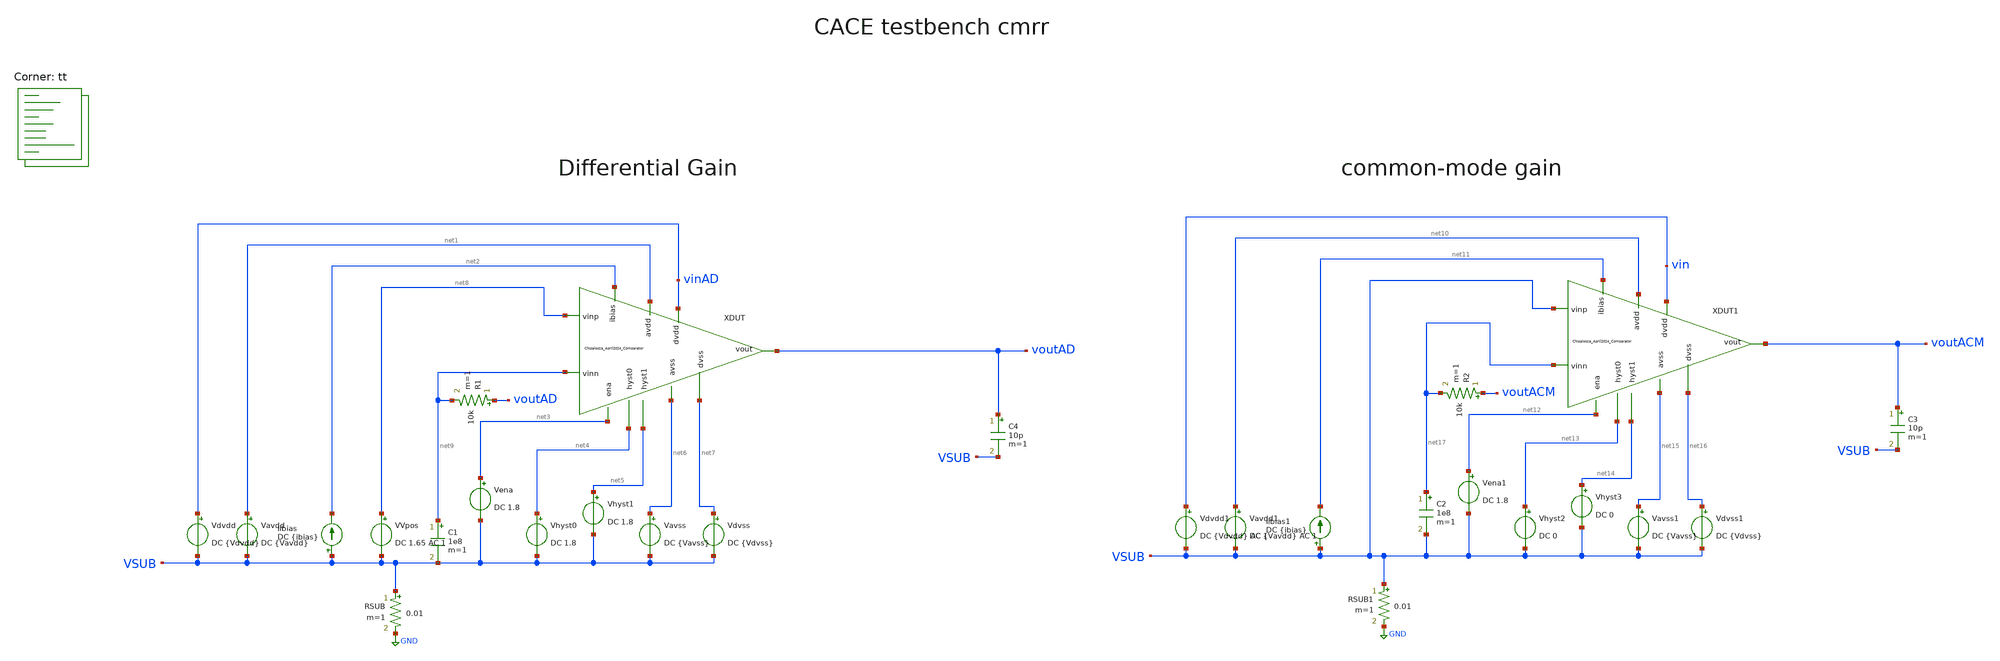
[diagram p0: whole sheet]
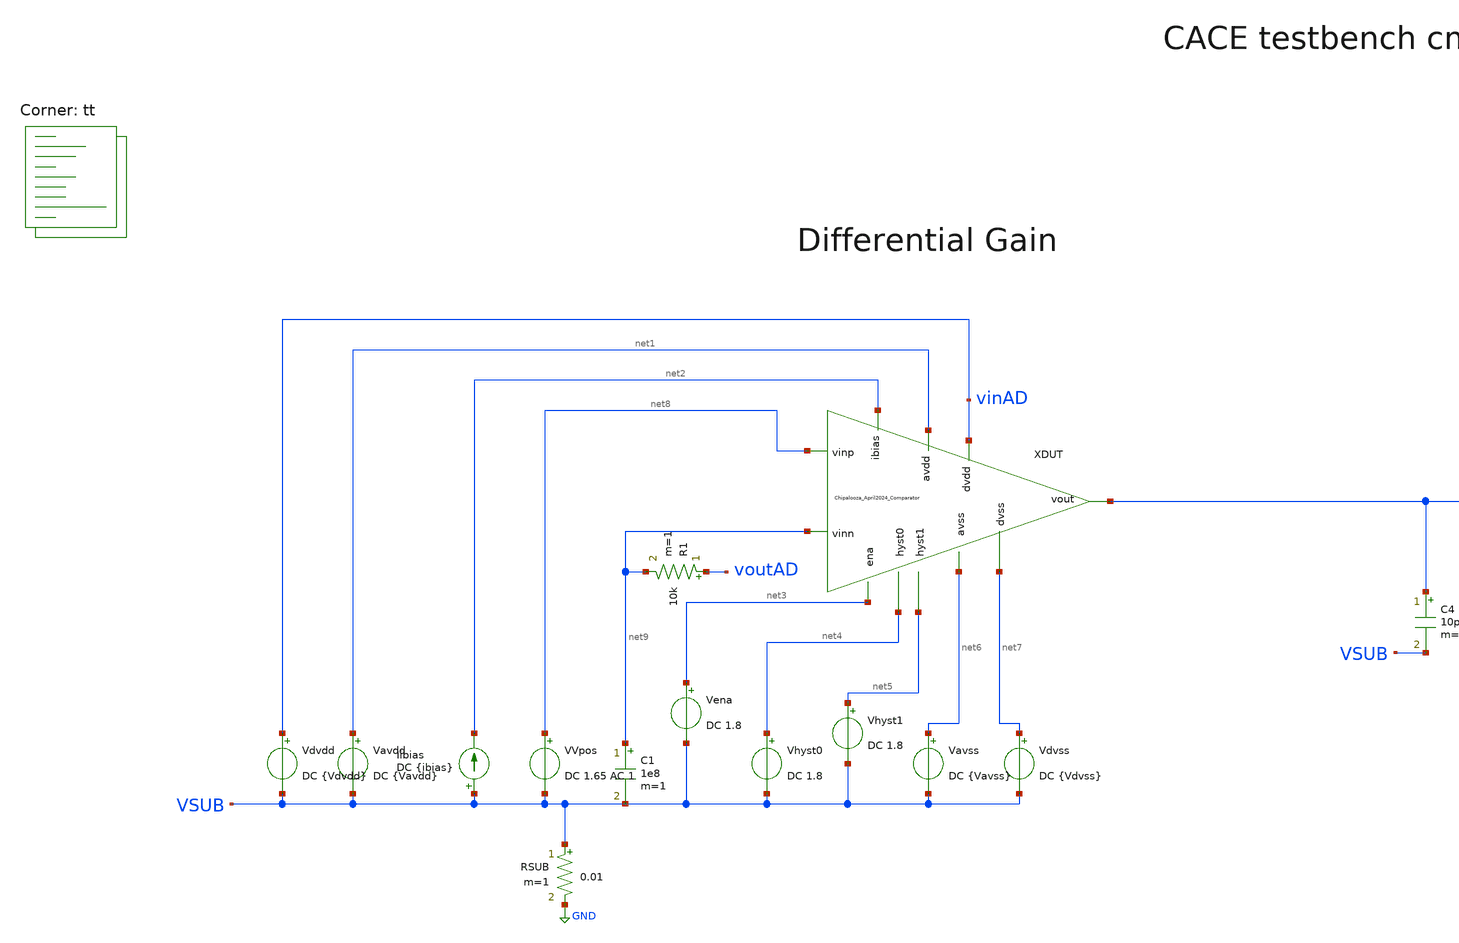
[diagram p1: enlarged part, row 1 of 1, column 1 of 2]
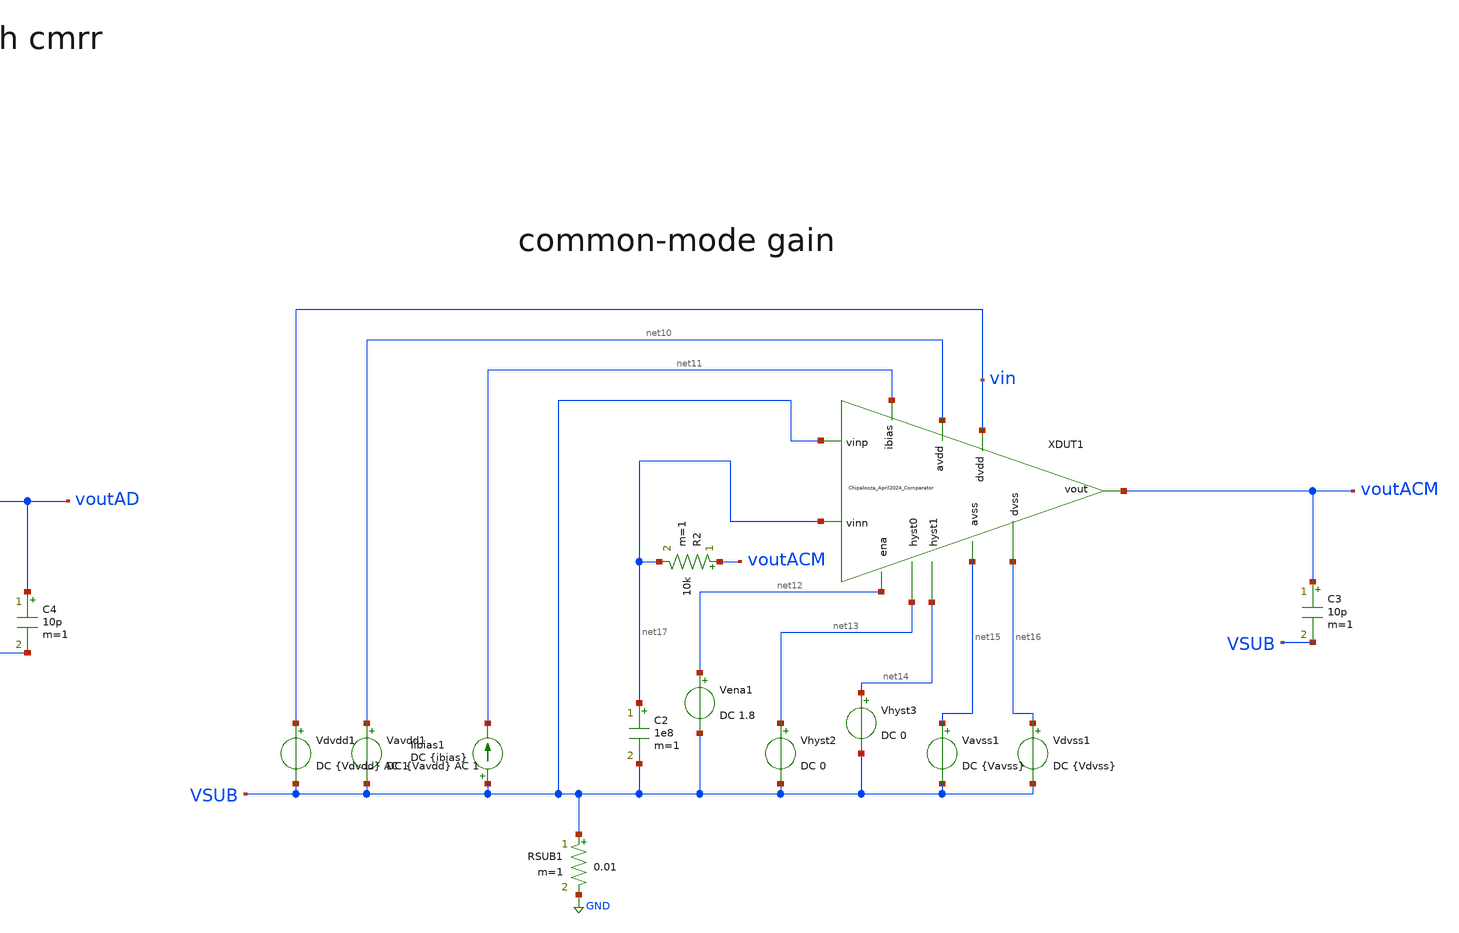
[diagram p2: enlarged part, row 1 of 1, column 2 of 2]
** sch_path: Chipalooza_April2024_Comparator/xschem/TB_psrr.sch
**.subckt TB_psrr
Vavdd net1 VSUB DC {Vavdd}
Vdvdd vinAD VSUB DC {Vdvdd}
Vena net3 VSUB DC 1.8
Vhyst0 net4 VSUB DC 1.8
Vhyst1 net5 VSUB DC 1.8
Vavss net6 VSUB DC {Vavss}
Vdvss net7 VSUB DC {Vdvss}
RSUB VSUB GND 0.01 m=1
Iibias VSUB net2 DC {ibias}
XDUT net4 net5 net1 net8 net6 net9 vinAD net7 voutAD net2 net3 Chipalooza_April2024_Comparator
VVpos net8 VSUB DC 1.65 AC 1
C1 net9 VSUB 1e8 m=1
R1 voutAD net9 10k m=1
C4 voutAD VSUB 10p m=1
Vavdd1 net10 VSUB DC {Vavdd} AC 1
Vdvdd1 vin VSUB DC {Vdvdd} AC 1
Vena1 net12 VSUB DC 1.8
Vhyst2 net13 VSUB DC 0
Vhyst3 net14 VSUB DC 0
Vavss1 net15 VSUB DC {Vavss}
Vdvss1 net16 VSUB DC {Vdvss}
RSUB1 VSUB GND 0.01 m=1
Iibias1 VSUB net11 DC {ibias}
XDUT1 net13 net14 net10 VSUB net15 net17 vin net16 voutACM net11 net12
+ Chipalooza_April2024_Comparator
C3 voutACM VSUB 10p m=1
R2 voutACM net17 10k m=1
C2 net17 VSUB 1e8 m=1
**** begin user architecture code
.lib $::SKYWATER_MODELS/sky130.lib.spice tt

* this option enables mos model bin
* selection based on W/NF instead of W
*.option wnflag=1
.option savecurrents
.option save all
.option temp=25

.control

.param vdvdd=1.8 vavdd=3.3 rout=0 cout=1f
.param ibias=1u ena=1 Vhyst_0=1 Vhyst_1=1
.param vavss=0 vdvss=0


ac dec 20 1 1e12
plot V(voutACM)
plot db(V(voutACM))
plot db((V(voutACM)-V(voutAD))/(V(vin)-V(vinAD)))

write TB_cmrr.raw


*quit 0

.endc


**** end user architecture code
**.ends

* expanding   symbol:  Chipalooza_April2024_Comparator.sym # of pins=11
** sym_path: Chipalooza_April2024_Comparator/xschem/Chipalooza_April2024_Comparator.sym
** sch_path: Chipalooza_April2024_Comparator/xschem/Chipalooza_April2024_Comparator.sch
.subckt Chipalooza_April2024_Comparator hyst0 hyst1 avdd vinp avss vinn dvdd dvss vout ibias ena
*.ipin vinp
*.ipin vinn
*.ipin hyst0
*.ipin hyst1
*.ipin avdd
*.ipin avss
*.ipin dvdd
*.ipin dvss
*.opin vout
*.ipin ena
*.ipin ibias
XM29 SumOutBar SumOut dvdd dvdd sky130_fd_pr__pfet_01v8 L=1 W=4 nf=1 ad='int((nf+1)/2) * W/nf * 0.29'
+ as='int((nf+2)/2) * W/nf * 0.29' pd='2*int((nf+1)/2) * (W/nf + 0.29)' ps='2*int((nf+2)/2) * (W/nf + 0.29)'
+ nrd='0.29 / W' nrs='0.29 / W' sa=0 sb=0 sd=0 mult=2 m=2
XM30 SumOutBar SumOut avssi dvss sky130_fd_pr__nfet_01v8 L=1 W=2 nf=1 ad='int((nf+1)/2) * W/nf * 0.29'
+ as='int((nf+2)/2) * W/nf * 0.29' pd='2*int((nf+1)/2) * (W/nf + 0.29)' ps='2*int((nf+2)/2) * (W/nf + 0.29)'
+ nrd='0.29 / W' nrs='0.29 / W' sa=0 sb=0 sd=0 mult=2 m=2
XM25 net3 ibias avssi avss sky130_fd_pr__nfet_g5v0d10v5 L=4 W=1 nf=1 ad='int((nf+1)/2) * W/nf * 0.29'
+ as='int((nf+2)/2) * W/nf * 0.29' pd='2*int((nf+1)/2) * (W/nf + 0.29)' ps='2*int((nf+2)/2) * (W/nf + 0.29)'
+ nrd='0.29 / W' nrs='0.29 / W' sa=0 sb=0 sd=0 mult=2 m=2
C1 avss 0 2p m=1
XM39 net4 ibias avssi avss sky130_fd_pr__nfet_g5v0d10v5 L=1 W=1 nf=1 ad='int((nf+1)/2) * W/nf * 0.29'
+ as='int((nf+2)/2) * W/nf * 0.29' pd='2*int((nf+1)/2) * (W/nf + 0.29)' ps='2*int((nf+2)/2) * (W/nf + 0.29)'
+ nrd='0.29 / W' nrs='0.29 / W' sa=0 sb=0 sd=0 mult=2 m=2
XM16 vout SumOutBar dvdd dvdd sky130_fd_pr__pfet_01v8 L=1 W=4 nf=1 ad='int((nf+1)/2) * W/nf * 0.29' as='int((nf+2)/2) * W/nf * 0.29'
+ pd='2*int((nf+1)/2) * (W/nf + 0.29)' ps='2*int((nf+2)/2) * (W/nf + 0.29)' nrd='0.29 / W' nrs='0.29 / W'
+ sa=0 sb=0 sd=0 mult=2 m=2
XM18 vout SumOutBar avssi dvss sky130_fd_pr__nfet_01v8 L=1 W=2 nf=1 ad='int((nf+1)/2) * W/nf * 0.29'
+ as='int((nf+2)/2) * W/nf * 0.29' pd='2*int((nf+1)/2) * (W/nf + 0.29)' ps='2*int((nf+2)/2) * (W/nf + 0.29)'
+ nrd='0.29 / W' nrs='0.29 / W' sa=0 sb=0 sd=0 mult=2 m=2
XM4 SourceBias2 SourceBias2 avdd avdd sky130_fd_pr__pfet_g5v0d10v5 L=1 W=48 nf=1 ad='int((nf+1)/2) * W/nf * 0.29'
+ as='int((nf+2)/2) * W/nf * 0.29' pd='2*int((nf+1)/2) * (W/nf + 0.29)' ps='2*int((nf+2)/2) * (W/nf + 0.29)'
+ nrd='0.29 / W' nrs='0.29 / W' sa=0 sb=0 sd=0 mult=2 m=2
XM5 N1 SourceBias2 avdd avdd sky130_fd_pr__pfet_g5v0d10v5 L=1 W=48 nf=1 ad='int((nf+1)/2) * W/nf * 0.29'
+ as='int((nf+2)/2) * W/nf * 0.29' pd='2*int((nf+1)/2) * (W/nf + 0.29)' ps='2*int((nf+2)/2) * (W/nf + 0.29)'
+ nrd='0.29 / W' nrs='0.29 / W' sa=0 sb=0 sd=0 mult=2 m=2
XM6 N2 SourceBias2 avdd avdd sky130_fd_pr__pfet_g5v0d10v5 L=1 W=48 nf=1 ad='int((nf+1)/2) * W/nf * 0.29'
+ as='int((nf+2)/2) * W/nf * 0.29' pd='2*int((nf+1)/2) * (W/nf + 0.29)' ps='2*int((nf+2)/2) * (W/nf + 0.29)'
+ nrd='0.29 / W' nrs='0.29 / W' sa=0 sb=0 sd=0 mult=2 m=2
XM7 SumOut net5 N2 avdd sky130_fd_pr__pfet_g5v0d10v5 L=1 W=48 nf=1 ad='int((nf+1)/2) * W/nf * 0.29' as='int((nf+2)/2) * W/nf * 0.29'
+ pd='2*int((nf+1)/2) * (W/nf + 0.29)' ps='2*int((nf+2)/2) * (W/nf + 0.29)' nrd='0.29 / W' nrs='0.29 / W'
+ sa=0 sb=0 sd=0 mult=2 m=2
XM8 Sum net5 N1 avdd sky130_fd_pr__pfet_g5v0d10v5 L=1 W=48 nf=1 ad='int((nf+1)/2) * W/nf * 0.29' as='int((nf+2)/2) * W/nf * 0.29'
+ pd='2*int((nf+1)/2) * (W/nf + 0.29)' ps='2*int((nf+2)/2) * (W/nf + 0.29)' nrd='0.29 / W' nrs='0.29 / W'
+ sa=0 sb=0 sd=0 mult=2 m=2
XM9 SumOut net6 P2 avss sky130_fd_pr__nfet_g5v0d10v5 L=3 W=12 nf=1 ad='int((nf+1)/2) * W/nf * 0.29' as='int((nf+2)/2) * W/nf * 0.29'
+ pd='2*int((nf+1)/2) * (W/nf + 0.29)' ps='2*int((nf+2)/2) * (W/nf + 0.29)' nrd='0.29 / W' nrs='0.29 / W'
+ sa=0 sb=0 sd=0 mult=2 m=2
XM10 Sum net6 P1 avss sky130_fd_pr__nfet_g5v0d10v5 L=3 W=12 nf=1 ad='int((nf+1)/2) * W/nf * 0.29' as='int((nf+2)/2) * W/nf * 0.29'
+ pd='2*int((nf+1)/2) * (W/nf + 0.29)' ps='2*int((nf+2)/2) * (W/nf + 0.29)' nrd='0.29 / W' nrs='0.29 / W'
+ sa=0 sb=0 sd=0 mult=2 m=2
XM11 P2 Sum avssi avss sky130_fd_pr__nfet_g5v0d10v5 L=3 W=12 nf=1 ad='int((nf+1)/2) * W/nf * 0.29' as='int((nf+2)/2) * W/nf * 0.29'
+ pd='2*int((nf+1)/2) * (W/nf + 0.29)' ps='2*int((nf+2)/2) * (W/nf + 0.29)' nrd='0.29 / W' nrs='0.29 / W'
+ sa=0 sb=0 sd=0 mult=2 m=2
XM12 P1 Sum avssi avss sky130_fd_pr__nfet_g5v0d10v5 L=3 W=12 nf=1 ad='int((nf+1)/2) * W/nf * 0.29' as='int((nf+2)/2) * W/nf * 0.29'
+ pd='2*int((nf+1)/2) * (W/nf + 0.29)' ps='2*int((nf+2)/2) * (W/nf + 0.29)' nrd='0.29 / W' nrs='0.29 / W'
+ sa=0 sb=0 sd=0 mult=2 m=2
XM2 P2 vinn psource_input avdd sky130_fd_pr__pfet_g5v0d10v5 L=1 W=16 nf=1 ad='int((nf+1)/2) * W/nf * 0.29'
+ as='int((nf+2)/2) * W/nf * 0.29' pd='2*int((nf+1)/2) * (W/nf + 0.29)' ps='2*int((nf+2)/2) * (W/nf + 0.29)'
+ nrd='0.29 / W' nrs='0.29 / W' sa=0 sb=0 sd=0 mult=2 m=2
XM3 P1 vinp psource_input avdd sky130_fd_pr__pfet_g5v0d10v5 L=1 W=16 nf=1 ad='int((nf+1)/2) * W/nf * 0.29'
+ as='int((nf+2)/2) * W/nf * 0.29' pd='2*int((nf+1)/2) * (W/nf + 0.29)' ps='2*int((nf+2)/2) * (W/nf + 0.29)'
+ nrd='0.29 / W' nrs='0.29 / W' sa=0 sb=0 sd=0 mult=2 m=2
XM14 psource_input pbias_tail avdd avdd sky130_fd_pr__pfet_g5v0d10v5 L=1 W=12 nf=1 ad='int((nf+1)/2) * W/nf * 0.29'
+ as='int((nf+2)/2) * W/nf * 0.29' pd='2*int((nf+1)/2) * (W/nf + 0.29)' ps='2*int((nf+2)/2) * (W/nf + 0.29)'
+ nrd='0.29 / W' nrs='0.29 / W' sa=0 sb=0 sd=0 mult=2 m=2
XM15 pbias_tail pbias_tail avdd avdd sky130_fd_pr__pfet_g5v0d10v5 L=1 W=6 nf=1 ad='int((nf+1)/2) * W/nf * 0.29'
+ as='int((nf+2)/2) * W/nf * 0.29' pd='2*int((nf+1)/2) * (W/nf + 0.29)' ps='2*int((nf+2)/2) * (W/nf + 0.29)'
+ nrd='0.29 / W' nrs='0.29 / W' sa=0 sb=0 sd=0 mult=2 m=2
XM17 nbias_tail net14 psource_input avdd sky130_fd_pr__pfet_g5v0d10v5 L=1 W=6 nf=1 ad='int((nf+1)/2) * W/nf * 0.29'
+ as='int((nf+2)/2) * W/nf * 0.29' pd='2*int((nf+1)/2) * (W/nf + 0.29)' ps='2*int((nf+2)/2) * (W/nf + 0.29)'
+ nrd='0.29 / W' nrs='0.29 / W' sa=0 sb=0 sd=0 mult=2 m=2
XM20 N1 vinp SourceBias0 avss sky130_fd_pr__nfet_g5v0d10v5 L=1 W=8 nf=1 ad='int((nf+1)/2) * W/nf * 0.29'
+ as='int((nf+2)/2) * W/nf * 0.29' pd='2*int((nf+1)/2) * (W/nf + 0.29)' ps='2*int((nf+2)/2) * (W/nf + 0.29)'
+ nrd='0.29 / W' nrs='0.29 / W' sa=0 sb=0 sd=0 mult=2 m=2
XM21 N2 vinn SourceBias0 avss sky130_fd_pr__nfet_g5v0d10v5 L=1 W=8 nf=1 ad='int((nf+1)/2) * W/nf * 0.29'
+ as='int((nf+2)/2) * W/nf * 0.29' pd='2*int((nf+1)/2) * (W/nf + 0.29)' ps='2*int((nf+2)/2) * (W/nf + 0.29)'
+ nrd='0.29 / W' nrs='0.29 / W' sa=0 sb=0 sd=0 mult=2 m=2
XM22 SourceBias0 nbias_tail avssi avss sky130_fd_pr__nfet_g5v0d10v5 L=1 W=9 nf=1 ad='int((nf+1)/2) * W/nf * 0.29'
+ as='int((nf+2)/2) * W/nf * 0.29' pd='2*int((nf+1)/2) * (W/nf + 0.29)' ps='2*int((nf+2)/2) * (W/nf + 0.29)'
+ nrd='0.29 / W' nrs='0.29 / W' sa=0 sb=0 sd=0 mult=2 m=2
XM23 nbias_tail nbias_tail avssi avss sky130_fd_pr__nfet_g5v0d10v5 L=1 W=3 nf=1 ad='int((nf+1)/2) * W/nf * 0.29'
+ as='int((nf+2)/2) * W/nf * 0.29' pd='2*int((nf+1)/2) * (W/nf + 0.29)' ps='2*int((nf+2)/2) * (W/nf + 0.29)'
+ nrd='0.29 / W' nrs='0.29 / W' sa=0 sb=0 sd=0 mult=2 m=2
XM28 pbias_tail net7 SourceBias0 avss sky130_fd_pr__nfet_g5v0d10v5 L=1 W=3 nf=1 ad='int((nf+1)/2) * W/nf * 0.29'
+ as='int((nf+2)/2) * W/nf * 0.29' pd='2*int((nf+1)/2) * (W/nf + 0.29)' ps='2*int((nf+2)/2) * (W/nf + 0.29)'
+ nrd='0.29 / W' nrs='0.29 / W' sa=0 sb=0 sd=0 mult=2 m=2
XM45 SourceBias1 ibias avssi avss sky130_fd_pr__nfet_g5v0d10v5 L=1 W=3 nf=1 ad='int((nf+1)/2) * W/nf * 0.29'
+ as='int((nf+2)/2) * W/nf * 0.29' pd='2*int((nf+1)/2) * (W/nf + 0.29)' ps='2*int((nf+2)/2) * (W/nf + 0.29)'
+ nrd='0.29 / W' nrs='0.29 / W' sa=0 sb=0 sd=0 mult=2 m=2
XM46 SourceBias1 SourceBias1 avdd avdd sky130_fd_pr__pfet_g5v0d10v5 L=1 W=6 nf=1 ad='int((nf+1)/2) * W/nf * 0.29'
+ as='int((nf+2)/2) * W/nf * 0.29' pd='2*int((nf+1)/2) * (W/nf + 0.29)' ps='2*int((nf+2)/2) * (W/nf + 0.29)'
+ nrd='0.29 / W' nrs='0.29 / W' sa=0 sb=0 sd=0 mult=2 m=2
XM47 psource_input SourceBias1 avdd avdd sky130_fd_pr__pfet_g5v0d10v5 L=1 W=6 nf=1 ad='int((nf+1)/2) * W/nf * 0.29'
+ as='int((nf+2)/2) * W/nf * 0.29' pd='2*int((nf+1)/2) * (W/nf + 0.29)' ps='2*int((nf+2)/2) * (W/nf + 0.29)'
+ nrd='0.29 / W' nrs='0.29 / W' sa=0 sb=0 sd=0 mult=2 m=2
XM48 SourceBias2 ibias avssi avss sky130_fd_pr__nfet_g5v0d10v5 L=1 W=6 nf=1 ad='int((nf+1)/2) * W/nf * 0.29'
+ as='int((nf+2)/2) * W/nf * 0.29' pd='2*int((nf+1)/2) * (W/nf + 0.29)' ps='2*int((nf+2)/2) * (W/nf + 0.29)'
+ nrd='0.29 / W' nrs='0.29 / W' sa=0 sb=0 sd=0 mult=2 m=2
XM65 SourceBias3 ibias avssi avss sky130_fd_pr__nfet_g5v0d10v5 L=1 W=1 nf=1 ad='int((nf+1)/2) * W/nf * 0.29'
+ as='int((nf+2)/2) * W/nf * 0.29' pd='2*int((nf+1)/2) * (W/nf + 0.29)' ps='2*int((nf+2)/2) * (W/nf + 0.29)'
+ nrd='0.29 / W' nrs='0.29 / W' sa=0 sb=0 sd=0 mult=2 m=2
XM76 Bias1 ibias avssi avss sky130_fd_pr__nfet_g5v0d10v5 L=1 W=3 nf=1 ad='int((nf+1)/2) * W/nf * 0.29'
+ as='int((nf+2)/2) * W/nf * 0.29' pd='2*int((nf+1)/2) * (W/nf + 0.29)' ps='2*int((nf+2)/2) * (W/nf + 0.29)'
+ nrd='0.29 / W' nrs='0.29 / W' sa=0 sb=0 sd=0 mult=2 m=2
XM77 SourceBias5 ibias avssi avss sky130_fd_pr__nfet_g5v0d10v5 L=1 W=3 nf=1 ad='int((nf+1)/2) * W/nf * 0.29'
+ as='int((nf+2)/2) * W/nf * 0.29' pd='2*int((nf+1)/2) * (W/nf + 0.29)' ps='2*int((nf+2)/2) * (W/nf + 0.29)'
+ nrd='0.29 / W' nrs='0.29 / W' sa=0 sb=0 sd=0 mult=2 m=2
XM78 SourceBias6 ibias avssi avss sky130_fd_pr__nfet_g5v0d10v5 L=1 W=3 nf=1 ad='int((nf+1)/2) * W/nf * 0.29'
+ as='int((nf+2)/2) * W/nf * 0.29' pd='2*int((nf+1)/2) * (W/nf + 0.29)' ps='2*int((nf+2)/2) * (W/nf + 0.29)'
+ nrd='0.29 / W' nrs='0.29 / W' sa=0 sb=0 sd=0 mult=2 m=2
XM79 SourceBias7 ibias avssi avss sky130_fd_pr__nfet_g5v0d10v5 L=1 W=3 nf=1 ad='int((nf+1)/2) * W/nf * 0.29'
+ as='int((nf+2)/2) * W/nf * 0.29' pd='2*int((nf+1)/2) * (W/nf + 0.29)' ps='2*int((nf+2)/2) * (W/nf + 0.29)'
+ nrd='0.29 / W' nrs='0.29 / W' sa=0 sb=0 sd=0 mult=2 m=2
XM81 Bias5 ibias avssi avss sky130_fd_pr__nfet_g5v0d10v5 L=1 W=3 nf=1 ad='int((nf+1)/2) * W/nf * 0.29'
+ as='int((nf+2)/2) * W/nf * 0.29' pd='2*int((nf+1)/2) * (W/nf + 0.29)' ps='2*int((nf+2)/2) * (W/nf + 0.29)'
+ nrd='0.29 / W' nrs='0.29 / W' sa=0 sb=0 sd=0 mult=2 m=2
XM54 M55Source M55Drain avssi avss sky130_fd_pr__nfet_g5v0d10v5 L=1.5 W=6 nf=1 ad='int((nf+1)/2) * W/nf * 0.29'
+ as='int((nf+2)/2) * W/nf * 0.29' pd='2*int((nf+1)/2) * (W/nf + 0.29)' ps='2*int((nf+2)/2) * (W/nf + 0.29)'
+ nrd='0.29 / W' nrs='0.29 / W' sa=0 sb=0 sd=0 mult=2 m=2
XM55 M55Drain Bias2 M55Source avss sky130_fd_pr__nfet_g5v0d10v5 L=1 W=9 nf=1 ad='int((nf+1)/2) * W/nf * 0.29'
+ as='int((nf+2)/2) * W/nf * 0.29' pd='2*int((nf+1)/2) * (W/nf + 0.29)' ps='2*int((nf+2)/2) * (W/nf + 0.29)'
+ nrd='0.29 / W' nrs='0.29 / W' sa=0 sb=0 sd=0 mult=2 m=2
XM56 Bias2 Bias2 avssi avss sky130_fd_pr__nfet_g5v0d10v5 L=2 W=0.5 nf=1 ad='int((nf+1)/2) * W/nf * 0.29'
+ as='int((nf+2)/2) * W/nf * 0.29' pd='2*int((nf+1)/2) * (W/nf + 0.29)' ps='2*int((nf+2)/2) * (W/nf + 0.29)'
+ nrd='0.29 / W' nrs='0.29 / W' sa=0 sb=0 sd=0 mult=1 m=1
XM51 net8 net9 avdd avdd sky130_fd_pr__pfet_g5v0d10v5 L=2 W=20 nf=1 ad='int((nf+1)/2) * W/nf * 0.29'
+ as='int((nf+2)/2) * W/nf * 0.29' pd='2*int((nf+1)/2) * (W/nf + 0.29)' ps='2*int((nf+2)/2) * (W/nf + 0.29)'
+ nrd='0.29 / W' nrs='0.29 / W' sa=0 sb=0 sd=0 mult=2 m=2
XM49 net9 net9 avdd avdd sky130_fd_pr__pfet_g5v0d10v5 L=2 W=10 nf=1 ad='int((nf+1)/2) * W/nf * 0.29'
+ as='int((nf+2)/2) * W/nf * 0.29' pd='2*int((nf+1)/2) * (W/nf + 0.29)' ps='2*int((nf+2)/2) * (W/nf + 0.29)'
+ nrd='0.29 / W' nrs='0.29 / W' sa=0 sb=0 sd=0 mult=2 m=2
XM50 SourceBias4 SourceBias4 net9 avdd sky130_fd_pr__pfet_g5v0d10v5 L=1 W=10 nf=1 ad='int((nf+1)/2) * W/nf * 0.29'
+ as='int((nf+2)/2) * W/nf * 0.29' pd='2*int((nf+1)/2) * (W/nf + 0.29)' ps='2*int((nf+2)/2) * (W/nf + 0.29)'
+ nrd='0.29 / W' nrs='0.29 / W' sa=0 sb=0 sd=0 mult=2 m=2
XM52 avssi SourceBias4 net8 avdd sky130_fd_pr__pfet_g5v0d10v5 L=1 W=1 nf=1 ad='int((nf+1)/2) * W/nf * 0.29'
+ as='int((nf+2)/2) * W/nf * 0.29' pd='2*int((nf+1)/2) * (W/nf + 0.29)' ps='2*int((nf+2)/2) * (W/nf + 0.29)'
+ nrd='0.29 / W' nrs='0.29 / W' sa=0 sb=0 sd=0 mult=2 m=2
XM53 Bias1 Bias1 net8 avdd sky130_fd_pr__pfet_g5v0d10v5 L=1 W=5 nf=1 ad='int((nf+1)/2) * W/nf * 0.29'
+ as='int((nf+2)/2) * W/nf * 0.29' pd='2*int((nf+1)/2) * (W/nf + 0.29)' ps='2*int((nf+2)/2) * (W/nf + 0.29)'
+ nrd='0.29 / W' nrs='0.29 / W' sa=0 sb=0 sd=0 mult=2 m=2
XM66 net10 net11 avdd avdd sky130_fd_pr__pfet_g5v0d10v5 L=2 W=20 nf=1 ad='int((nf+1)/2) * W/nf * 0.29'
+ as='int((nf+2)/2) * W/nf * 0.29' pd='2*int((nf+1)/2) * (W/nf + 0.29)' ps='2*int((nf+2)/2) * (W/nf + 0.29)'
+ nrd='0.29 / W' nrs='0.29 / W' sa=0 sb=0 sd=0 mult=2 m=2
XM67 net11 net11 avdd avdd sky130_fd_pr__pfet_g5v0d10v5 L=2 W=20 nf=1 ad='int((nf+1)/2) * W/nf * 0.29'
+ as='int((nf+2)/2) * W/nf * 0.29' pd='2*int((nf+1)/2) * (W/nf + 0.29)' ps='2*int((nf+2)/2) * (W/nf + 0.29)'
+ nrd='0.29 / W' nrs='0.29 / W' sa=0 sb=0 sd=0 mult=2 m=2
XM68 SourceBias7 SourceBias7 net11 avdd sky130_fd_pr__pfet_g5v0d10v5 L=1 W=10 nf=1 ad='int((nf+1)/2) * W/nf * 0.29'
+ as='int((nf+2)/2) * W/nf * 0.29' pd='2*int((nf+1)/2) * (W/nf + 0.29)' ps='2*int((nf+2)/2) * (W/nf + 0.29)'
+ nrd='0.29 / W' nrs='0.29 / W' sa=0 sb=0 sd=0 mult=2 m=2
XM69 avssi SourceBias7 net10 avdd sky130_fd_pr__pfet_g5v0d10v5 L=1 W=1 nf=1 ad='int((nf+1)/2) * W/nf * 0.29'
+ as='int((nf+2)/2) * W/nf * 0.29' pd='2*int((nf+1)/2) * (W/nf + 0.29)' ps='2*int((nf+2)/2) * (W/nf + 0.29)'
+ nrd='0.29 / W' nrs='0.29 / W' sa=0 sb=0 sd=0 mult=2 m=2
XM70 Bias5 Bias5 net10 avdd sky130_fd_pr__pfet_g5v0d10v5 L=1 W=5 nf=1 ad='int((nf+1)/2) * W/nf * 0.29'
+ as='int((nf+2)/2) * W/nf * 0.29' pd='2*int((nf+1)/2) * (W/nf + 0.29)' ps='2*int((nf+2)/2) * (W/nf + 0.29)'
+ nrd='0.29 / W' nrs='0.29 / W' sa=0 sb=0 sd=0 mult=2 m=2
XM72 SourceBias5 SourceBias5 avdd avdd sky130_fd_pr__pfet_g5v0d10v5 L=1 W=12 nf=1 ad='int((nf+1)/2) * W/nf * 0.29'
+ as='int((nf+2)/2) * W/nf * 0.29' pd='2*int((nf+1)/2) * (W/nf + 0.29)' ps='2*int((nf+2)/2) * (W/nf + 0.29)'
+ nrd='0.29 / W' nrs='0.29 / W' sa=0 sb=0 sd=0 mult=4 m=4
XM73 M55Drain SourceBias5 avdd avdd sky130_fd_pr__pfet_g5v0d10v5 L=1 W=12 nf=1 ad='int((nf+1)/2) * W/nf * 0.29'
+ as='int((nf+2)/2) * W/nf * 0.29' pd='2*int((nf+1)/2) * (W/nf + 0.29)' ps='2*int((nf+2)/2) * (W/nf + 0.29)'
+ nrd='0.29 / W' nrs='0.29 / W' sa=0 sb=0 sd=0 mult=4 m=4
XM74 SourceBias6 SourceBias6 avdd avdd sky130_fd_pr__pfet_g5v0d10v5 L=1 W=12 nf=1 ad='int((nf+1)/2) * W/nf * 0.29'
+ as='int((nf+2)/2) * W/nf * 0.29' pd='2*int((nf+1)/2) * (W/nf + 0.29)' ps='2*int((nf+2)/2) * (W/nf + 0.29)'
+ nrd='0.29 / W' nrs='0.29 / W' sa=0 sb=0 sd=0 mult=4 m=4
XM75 Bias2 SourceBias6 avdd avdd sky130_fd_pr__pfet_g5v0d10v5 L=1 W=12 nf=1 ad='int((nf+1)/2) * W/nf * 0.29'
+ as='int((nf+2)/2) * W/nf * 0.29' pd='2*int((nf+1)/2) * (W/nf + 0.29)' ps='2*int((nf+2)/2) * (W/nf + 0.29)'
+ nrd='0.29 / W' nrs='0.29 / W' sa=0 sb=0 sd=0 mult=4 m=4
XM1 SourceBias0 ibias avssi avss sky130_fd_pr__nfet_g5v0d10v5 L=1 W=3 nf=1 ad='int((nf+1)/2) * W/nf * 0.29'
+ as='int((nf+2)/2) * W/nf * 0.29' pd='2*int((nf+1)/2) * (W/nf + 0.29)' ps='2*int((nf+2)/2) * (W/nf + 0.29)'
+ nrd='0.29 / W' nrs='0.29 / W' sa=0 sb=0 sd=0 mult=2 m=2
XM31 net1 hyst0 net3 avss sky130_fd_pr__nfet_01v8 L=4 W=1 nf=1 ad='int((1 + 1)/2) * 1 / 1 * 0.29' as='int((1 + 2)/2) * 1 / 1 * 0.29'
+ pd='2*int((1 + 1)/2) * (1 / 1 + 0.29)' ps='2*int((1 + 2)/2) * (1 / 1 + 0.29)' nrd='0.29 / 1 ' nrs='0.29 / 1 '
+ sa=0 sb=0 sd=0 mult=2 m=2
XM32 net1 hyst1 net4 avss sky130_fd_pr__nfet_01v8 L=1 W=1 nf=1 ad='int((1 + 1)/2) * 1 / 1 * 0.29' as='int((1 + 2)/2) * 1 / 1 * 0.29'
+ pd='2*int((1 + 1)/2) * (1 / 1 + 0.29)' ps='2*int((1 + 2)/2) * (1 / 1 + 0.29)' nrd='0.29 / 1 ' nrs='0.29 / 1 '
+ sa=0 sb=0 sd=0 mult=2 m=2
XM19 avdd SumOut net1 avss sky130_fd_pr__nfet_g5v0d10v5 L=1 W=2 nf=1 ad='int((nf+1)/2) * W/nf * 0.29'
+ as='int((nf+2)/2) * W/nf * 0.29' pd='2*int((nf+1)/2) * (W/nf + 0.29)' ps='2*int((nf+2)/2) * (W/nf + 0.29)'
+ nrd='0.29 / W' nrs='0.29 / W' sa=0 sb=0 sd=0 mult=2 m=2
XM24 avdd SumOutBar net1 avss sky130_fd_pr__nfet_g5v0d10v5 L=1 W=2 nf=1 ad='int((nf+1)/2) * W/nf * 0.29'
+ as='int((nf+2)/2) * W/nf * 0.29' pd='2*int((nf+1)/2) * (W/nf + 0.29)' ps='2*int((nf+2)/2) * (W/nf + 0.29)'
+ nrd='0.29 / W' nrs='0.29 / W' sa=0 sb=0 sd=0 mult=2 m=2
XM26 ibias ibias avssi avss sky130_fd_pr__nfet_g5v0d10v5 L=1 W=3 nf=1 ad='int((nf+1)/2) * W/nf * 0.29'
+ as='int((nf+2)/2) * W/nf * 0.29' pd='2*int((nf+1)/2) * (W/nf + 0.29)' ps='2*int((nf+2)/2) * (W/nf + 0.29)'
+ nrd='0.29 / W' nrs='0.29 / W' sa=0 sb=0 sd=0 mult=2 m=2
XM27 net2 ibias avssi avss sky130_fd_pr__nfet_g5v0d10v5 L=1 W=3 nf=1 ad='int((nf+1)/2) * W/nf * 0.29'
+ as='int((nf+2)/2) * W/nf * 0.29' pd='2*int((nf+1)/2) * (W/nf + 0.29)' ps='2*int((nf+2)/2) * (W/nf + 0.29)'
+ nrd='0.29 / W' nrs='0.29 / W' sa=0 sb=0 sd=0 mult=2 m=2
XM33 net2 net2 avdd avdd sky130_fd_pr__pfet_g5v0d10v5 L=1 W=6 nf=1 ad='int((nf+1)/2) * W/nf * 0.29' as='int((nf+2)/2) * W/nf * 0.29'
+ pd='2*int((nf+1)/2) * (W/nf + 0.29)' ps='2*int((nf+2)/2) * (W/nf + 0.29)' nrd='0.29 / W' nrs='0.29 / W'
+ sa=0 sb=0 sd=0 mult=2 m=2
XM57 net12 net13 avdd avdd sky130_fd_pr__pfet_g5v0d10v5 L=2 W=20 nf=1 ad='int((nf+1)/2) * W/nf * 0.29'
+ as='int((nf+2)/2) * W/nf * 0.29' pd='2*int((nf+1)/2) * (W/nf + 0.29)' ps='2*int((nf+2)/2) * (W/nf + 0.29)'
+ nrd='0.29 / W' nrs='0.29 / W' sa=0 sb=0 sd=0 mult=2 m=2
XM58 net13 net13 avdd avdd sky130_fd_pr__pfet_g5v0d10v5 L=2 W=10 nf=1 ad='int((nf+1)/2) * W/nf * 0.29'
+ as='int((nf+2)/2) * W/nf * 0.29' pd='2*int((nf+1)/2) * (W/nf + 0.29)' ps='2*int((nf+2)/2) * (W/nf + 0.29)'
+ nrd='0.29 / W' nrs='0.29 / W' sa=0 sb=0 sd=0 mult=2 m=2
XM59 SourceBias10 SourceBias10 net13 avdd sky130_fd_pr__pfet_g5v0d10v5 L=1 W=10 nf=1 ad='int((nf+1)/2) * W/nf * 0.29'
+ as='int((nf+2)/2) * W/nf * 0.29' pd='2*int((nf+1)/2) * (W/nf + 0.29)' ps='2*int((nf+2)/2) * (W/nf + 0.29)'
+ nrd='0.29 / W' nrs='0.29 / W' sa=0 sb=0 sd=0 mult=2 m=2
XM60 avss SourceBias10 net12 avdd sky130_fd_pr__pfet_g5v0d10v5 L=1 W=1 nf=1 ad='int((nf+1)/2) * W/nf * 0.29'
+ as='int((nf+2)/2) * W/nf * 0.29' pd='2*int((nf+1)/2) * (W/nf + 0.29)' ps='2*int((nf+2)/2) * (W/nf + 0.29)'
+ nrd='0.29 / W' nrs='0.29 / W' sa=0 sb=0 sd=0 mult=2 m=2
XM61 Bias4 Bias4 net12 avdd sky130_fd_pr__pfet_g5v0d10v5 L=1 W=5 nf=1 ad='int((nf+1)/2) * W/nf * 0.29'
+ as='int((nf+2)/2) * W/nf * 0.29' pd='2*int((nf+1)/2) * (W/nf + 0.29)' ps='2*int((nf+2)/2) * (W/nf + 0.29)'
+ nrd='0.29 / W' nrs='0.29 / W' sa=0 sb=0 sd=0 mult=2 m=2
XM13 Bias4 ibias avssi avss sky130_fd_pr__nfet_g5v0d10v5 L=1 W=3 nf=1 ad='int((nf+1)/2) * W/nf * 0.29'
+ as='int((nf+2)/2) * W/nf * 0.29' pd='2*int((nf+1)/2) * (W/nf + 0.29)' ps='2*int((nf+2)/2) * (W/nf + 0.29)'
+ nrd='0.29 / W' nrs='0.29 / W' sa=0 sb=0 sd=0 mult=2 m=2
XM35 SourceBias10 ibias avssi avss sky130_fd_pr__nfet_g5v0d10v5 L=1 W=3 nf=1 ad='int((nf+1)/2) * W/nf * 0.29'
+ as='int((nf+2)/2) * W/nf * 0.29' pd='2*int((nf+1)/2) * (W/nf + 0.29)' ps='2*int((nf+2)/2) * (W/nf + 0.29)'
+ nrd='0.29 / W' nrs='0.29 / W' sa=0 sb=0 sd=0 mult=2 m=2
XM36 SourceBias4 ibias avssi avss sky130_fd_pr__nfet_g5v0d10v5 L=1 W=3 nf=1 ad='int((nf+1)/2) * W/nf * 0.29'
+ as='int((nf+2)/2) * W/nf * 0.29' pd='2*int((nf+1)/2) * (W/nf + 0.29)' ps='2*int((nf+2)/2) * (W/nf + 0.29)'
+ nrd='0.29 / W' nrs='0.29 / W' sa=0 sb=0 sd=0 mult=2 m=2
V1 net7 avssi 1.3
V2 net14 avssi 2
V3 net5 avssi 0
V4 net6 avssi 3.3
RSUB1 avssi avss 0.01 m=1
.ends

.GLOBAL GND
.end
